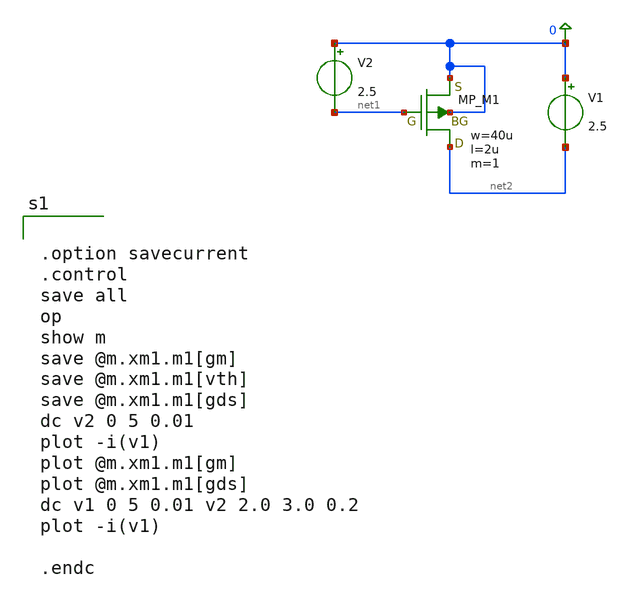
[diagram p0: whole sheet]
** sch_path: member_project/JJY_Receiver/Masahiro/jjy_recv/check_fet/pfet_gm.sch
**.subckt pfet_gm
XM1 net2 net1 0 0 PMOS w=40u l=2u as=0 ad=0 ps=0 pd=0 nrd=0 nrs=0 m=1
V1 0 net2 2.5
V2 0 net1 2.5
**** begin user architecture code
 .include $::LIB/ip62_models


.option savecurrent
.control
save all
op
show m
save @m.xm1.m1[gm]
save @m.xm1.m1[vth]
save @m.xm1.m1[gds]
dc v2 0 5 0.01
plot -i(v1)
plot @m.xm1.m1[gm]
plot @m.xm1.m1[gds]
dc v1 0 5 0.01 v2 2.0 3.0 0.2
plot -i(v1)

.endc


**** end user architecture code
**.ends
.end
